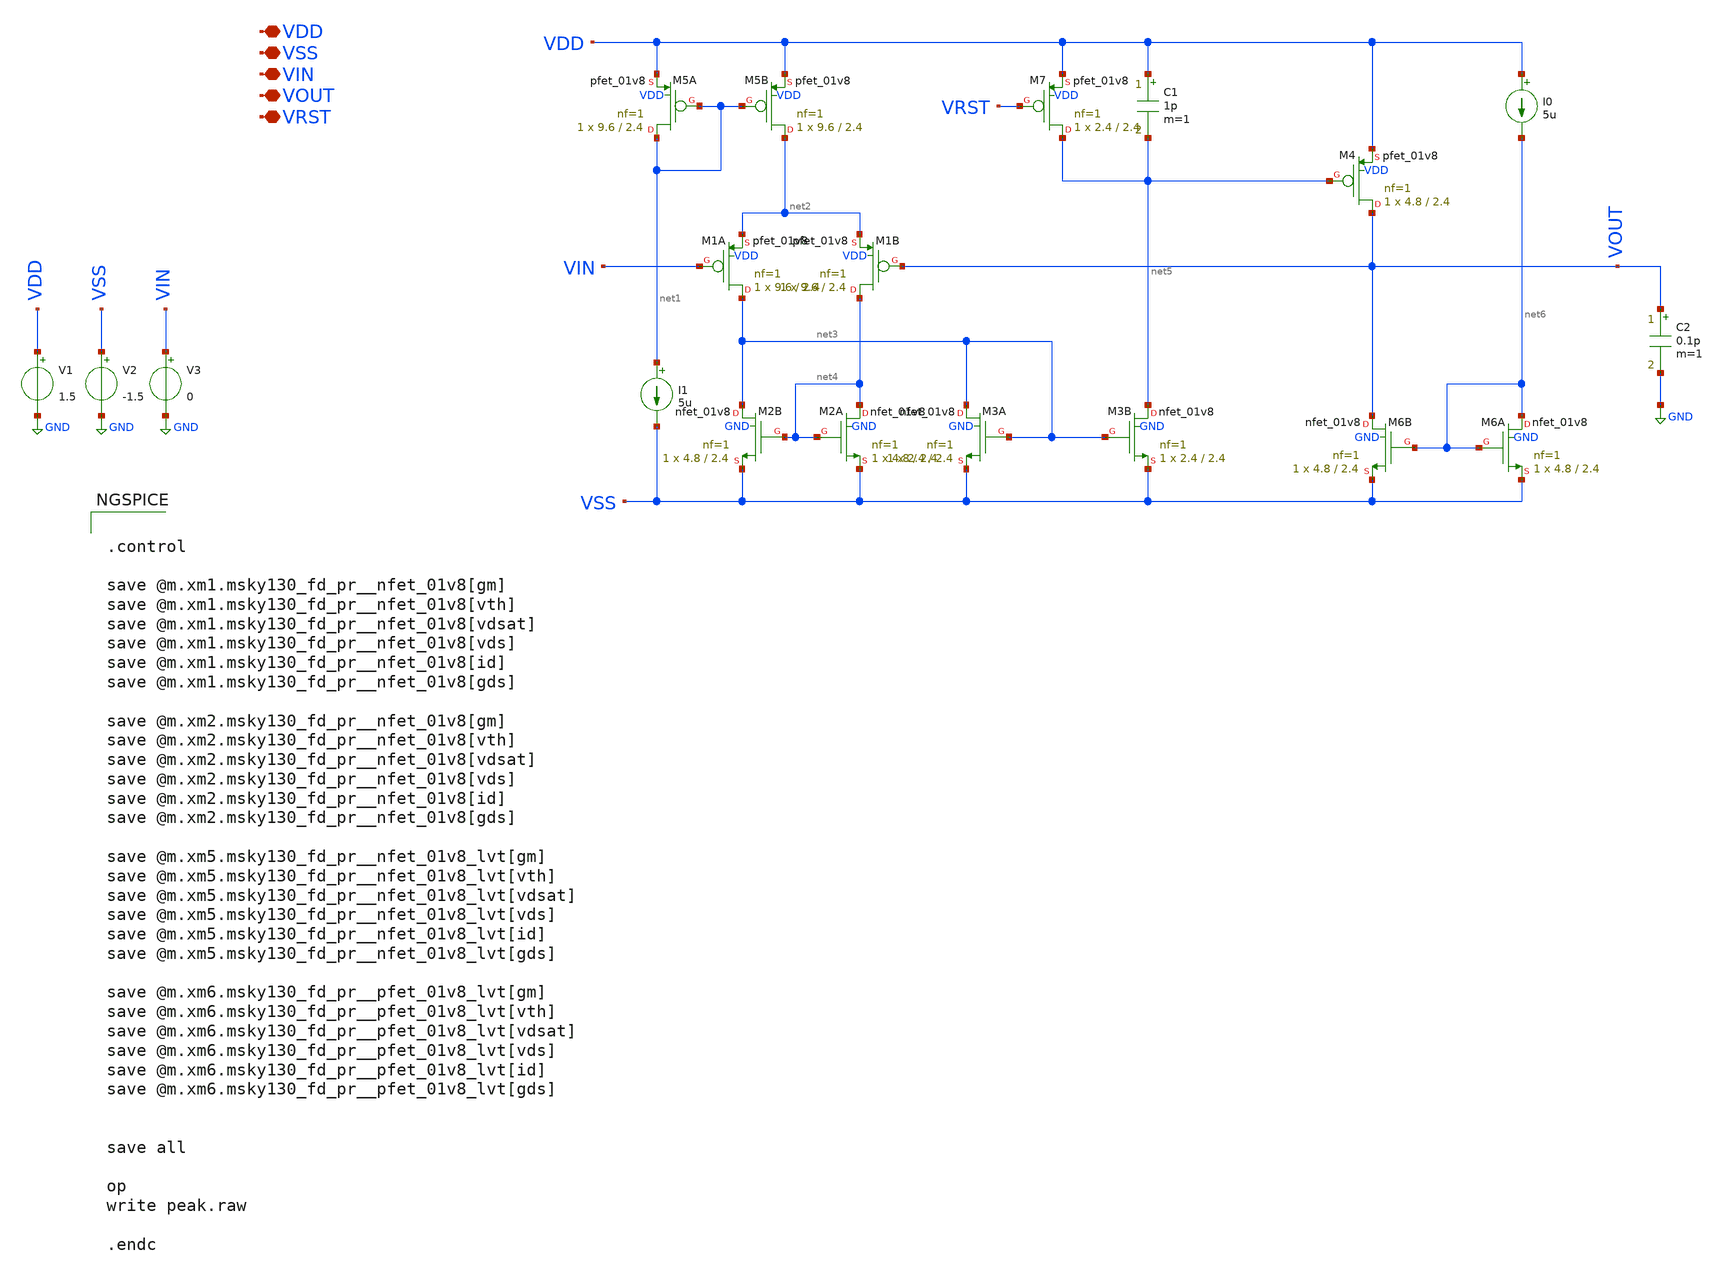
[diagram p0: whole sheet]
** sch_path: peak/peak.sch
**.subckt peak VDD VSS VIN VOUT VRST
*.iopin VDD
*.iopin VSS
*.iopin VIN
*.iopin VOUT
*.iopin VRST
C1 VDD net5 1p m=1
I0 VDD net6 5u
I1 net1 VSS 5u
V1 VDD GND 1.5
V2 VSS GND -1.5
V3 VIN GND 0
XM2B net3 net4 VSS GND sky130_fd_pr__nfet_01v8 L=2.4 W=4.8 nf=1 ad='int((nf+1)/2) * W/nf * 0.29' as='int((nf+2)/2) * W/nf * 0.29'
+ pd='2*int((nf+1)/2) * (W/nf + 0.29)' ps='2*int((nf+2)/2) * (W/nf + 0.29)' nrd='0.29 / W' nrs='0.29 / W'
+ sa=0 sb=0 sd=0 mult=1 m=1
XM3A net3 net3 VSS GND sky130_fd_pr__nfet_01v8 L=2.4 W=2.4 nf=1 ad='int((nf+1)/2) * W/nf * 0.29' as='int((nf+2)/2) * W/nf * 0.29'
+ pd='2*int((nf+1)/2) * (W/nf + 0.29)' ps='2*int((nf+2)/2) * (W/nf + 0.29)' nrd='0.29 / W' nrs='0.29 / W'
+ sa=0 sb=0 sd=0 mult=1 m=1
XM6B VOUT net6 VSS GND sky130_fd_pr__nfet_01v8 L=2.4 W=4.8 nf=1 ad='int((nf+1)/2) * W/nf * 0.29' as='int((nf+2)/2) * W/nf * 0.29'
+ pd='2*int((nf+1)/2) * (W/nf + 0.29)' ps='2*int((nf+2)/2) * (W/nf + 0.29)' nrd='0.29 / W' nrs='0.29 / W'
+ sa=0 sb=0 sd=0 mult=1 m=1
XM2A net4 net4 VSS GND sky130_fd_pr__nfet_01v8 L=2.4 W=4.8 nf=1 ad='int((nf+1)/2) * W/nf * 0.29' as='int((nf+2)/2) * W/nf * 0.29'
+ pd='2*int((nf+1)/2) * (W/nf + 0.29)' ps='2*int((nf+2)/2) * (W/nf + 0.29)' nrd='0.29 / W' nrs='0.29 / W'
+ sa=0 sb=0 sd=0 mult=1 m=1
XM3B net5 net3 VSS GND sky130_fd_pr__nfet_01v8 L=2.4 W=2.4 nf=1 ad='int((nf+1)/2) * W/nf * 0.29' as='int((nf+2)/2) * W/nf * 0.29'
+ pd='2*int((nf+1)/2) * (W/nf + 0.29)' ps='2*int((nf+2)/2) * (W/nf + 0.29)' nrd='0.29 / W' nrs='0.29 / W'
+ sa=0 sb=0 sd=0 mult=1 m=1
XM6A net6 net6 VSS GND sky130_fd_pr__nfet_01v8 L=2.4 W=4.8 nf=1 ad='int((nf+1)/2) * W/nf * 0.29' as='int((nf+2)/2) * W/nf * 0.29'
+ pd='2*int((nf+1)/2) * (W/nf + 0.29)' ps='2*int((nf+2)/2) * (W/nf + 0.29)' nrd='0.29 / W' nrs='0.29 / W'
+ sa=0 sb=0 sd=0 mult=1 m=1
XM5B net2 net1 VDD VDD sky130_fd_pr__pfet_01v8 L=2.4 W=9.6 nf=1 ad='int((nf+1)/2) * W/nf * 0.29' as='int((nf+2)/2) * W/nf * 0.29'
+ pd='2*int((nf+1)/2) * (W/nf + 0.29)' ps='2*int((nf+2)/2) * (W/nf + 0.29)' nrd='0.29 / W' nrs='0.29 / W'
+ sa=0 sb=0 sd=0 mult=1 m=1
XM5A net1 net1 VDD VDD sky130_fd_pr__pfet_01v8 L=2.4 W=9.6 nf=1 ad='int((nf+1)/2) * W/nf * 0.29' as='int((nf+2)/2) * W/nf * 0.29'
+ pd='2*int((nf+1)/2) * (W/nf + 0.29)' ps='2*int((nf+2)/2) * (W/nf + 0.29)' nrd='0.29 / W' nrs='0.29 / W'
+ sa=0 sb=0 sd=0 mult=1 m=1
XM7 net5 VRST VDD VDD sky130_fd_pr__pfet_01v8 L=2.4 W=2.4 nf=1 ad='int((nf+1)/2) * W/nf * 0.29' as='int((nf+2)/2) * W/nf * 0.29'
+ pd='2*int((nf+1)/2) * (W/nf + 0.29)' ps='2*int((nf+2)/2) * (W/nf + 0.29)' nrd='0.29 / W' nrs='0.29 / W'
+ sa=0 sb=0 sd=0 mult=1 m=1
XM4 VOUT net5 VDD VDD sky130_fd_pr__pfet_01v8 L=2.4 W=4.8 nf=1 ad='int((nf+1)/2) * W/nf * 0.29' as='int((nf+2)/2) * W/nf * 0.29'
+ pd='2*int((nf+1)/2) * (W/nf + 0.29)' ps='2*int((nf+2)/2) * (W/nf + 0.29)' nrd='0.29 / W' nrs='0.29 / W'
+ sa=0 sb=0 sd=0 mult=1 m=1
XM1B net4 VOUT net2 VDD sky130_fd_pr__pfet_01v8 L=2.4 W=9.6 nf=1 ad='int((nf+1)/2) * W/nf * 0.29' as='int((nf+2)/2) * W/nf * 0.29'
+ pd='2*int((nf+1)/2) * (W/nf + 0.29)' ps='2*int((nf+2)/2) * (W/nf + 0.29)' nrd='0.29 / W' nrs='0.29 / W'
+ sa=0 sb=0 sd=0 mult=1 m=1
XM1A net3 VIN net2 VDD sky130_fd_pr__pfet_01v8 L=2.4 W=9.6 nf=1 ad='int((nf+1)/2) * W/nf * 0.29' as='int((nf+2)/2) * W/nf * 0.29'
+ pd='2*int((nf+1)/2) * (W/nf + 0.29)' ps='2*int((nf+2)/2) * (W/nf + 0.29)' nrd='0.29 / W' nrs='0.29 / W'
+ sa=0 sb=0 sd=0 mult=1 m=1
C2 VOUT GND 0.1p m=1
**** begin user architecture code
 *


.control

save @m.xm1.msky130_fd_pr__nfet_01v8[gm]
save @m.xm1.msky130_fd_pr__nfet_01v8[vth]
save @m.xm1.msky130_fd_pr__nfet_01v8[vdsat]
save @m.xm1.msky130_fd_pr__nfet_01v8[vds]
save @m.xm1.msky130_fd_pr__nfet_01v8[id]
save @m.xm1.msky130_fd_pr__nfet_01v8[gds]

save @m.xm2.msky130_fd_pr__nfet_01v8[gm]
save @m.xm2.msky130_fd_pr__nfet_01v8[vth]
save @m.xm2.msky130_fd_pr__nfet_01v8[vdsat]
save @m.xm2.msky130_fd_pr__nfet_01v8[vds]
save @m.xm2.msky130_fd_pr__nfet_01v8[id]
save @m.xm2.msky130_fd_pr__nfet_01v8[gds]

save @m.xm5.msky130_fd_pr__nfet_01v8_lvt[gm]
save @m.xm5.msky130_fd_pr__nfet_01v8_lvt[vth]
save @m.xm5.msky130_fd_pr__nfet_01v8_lvt[vdsat]
save @m.xm5.msky130_fd_pr__nfet_01v8_lvt[vds]
save @m.xm5.msky130_fd_pr__nfet_01v8_lvt[id]
save @m.xm5.msky130_fd_pr__nfet_01v8_lvt[gds]

save @m.xm6.msky130_fd_pr__pfet_01v8_lvt[gm]
save @m.xm6.msky130_fd_pr__pfet_01v8_lvt[vth]
save @m.xm6.msky130_fd_pr__pfet_01v8_lvt[vdsat]
save @m.xm6.msky130_fd_pr__pfet_01v8_lvt[vds]
save @m.xm6.msky130_fd_pr__pfet_01v8_lvt[id]
save @m.xm6.msky130_fd_pr__pfet_01v8_lvt[gds]


save all

op
write peak.raw

.endc


**** end user architecture code
**.ends
.GLOBAL GND
.end
